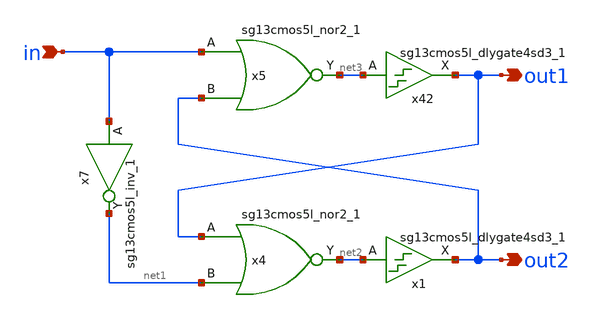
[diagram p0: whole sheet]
** sch_path: macros/heichips26_vcr/macros/switched_capacitor/schematic/xschem/deadtime_generator.sch
**.subckt deadtime_generator in out1 out2
*.ipin in
*.opin out1
*.opin out2
x4 net2 out1 net1 VDD VSS sg13cmos5l_nor2_1
x7 net1 in VDD VSS sg13cmos5l_inv_1
x5 net3 in out2 VDD VSS sg13cmos5l_nor2_1
x42 out1 net3 VDD VSS sg13cmos5l_dlygate4sd3_1
x1 out2 net2 VDD VSS sg13cmos5l_dlygate4sd3_1
**.ends
.end
